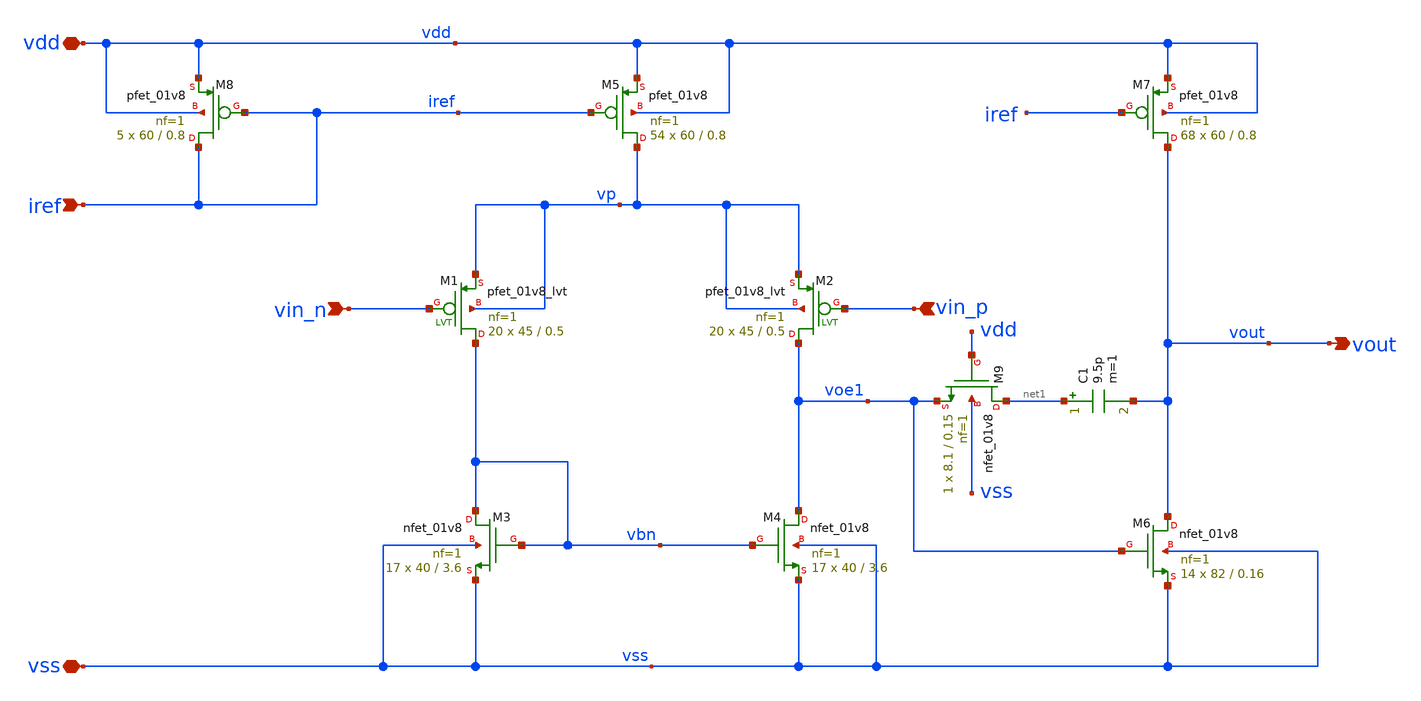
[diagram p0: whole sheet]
** sch_path: TpFinal/Mis Simulaciones/opamp.sch
**.subckt opamp vdd vss vin_n vin_p iref vout
*.iopin vdd
*.iopin vss
*.ipin vin_n
*.ipin vin_p
*.ipin iref
*.opin vout
XM3 vbn vbn vss vss sky130_fd_pr__nfet_01v8 L=3.6 W=40 nf=1 ad='W * 0.29' as='W * 0.29' pd='2 * (W + 0.29)'
+ ps='2 * (W + 0.29)' nrd='0.29 / W' nrs='0.29 / W' sa=0 sb=0 sd=0 mult=17 m=17
XM4 voe1 vbn vss vss sky130_fd_pr__nfet_01v8 L=3.6 W=40 nf=1 ad='W * 0.29' as='W * 0.29' pd='2 * (W + 0.29)'
+ ps='2 * (W + 0.29)' nrd='0.29 / W' nrs='0.29 / W' sa=0 sb=0 sd=0 mult=17 m=17
XM5 vp iref vdd vdd sky130_fd_pr__pfet_01v8 L=0.8 W=60 nf=1 ad='W * 0.29' as='W * 0.29' pd='2 * (W + 0.29)'
+ ps='2 * (W + 0.29)' nrd='0.29 / W' nrs='0.29 / W' sa=0 sb=0 sd=0 mult=54 m=54
XM7 vout iref vdd vdd sky130_fd_pr__pfet_01v8 L=0.8 W=60 nf=1 ad='W * 0.29' as='W * 0.29' pd='2 * (W + 0.29)'
+ ps='2 * (W + 0.29)' nrd='0.29 / W' nrs='0.29 / W' sa=0 sb=0 sd=0 mult=68 m=68
XM8 iref iref vdd vdd sky130_fd_pr__pfet_01v8 L=0.8 W=60 nf=1 ad='W * 0.29' as='W * 0.29' pd='2 * (W + 0.29)'
+ ps='2 * (W + 0.29)' nrd='0.29 / W' nrs='0.29 / W' sa=0 sb=0 sd=0 mult=5 m=5
XM9 net1 vdd voe1 vss sky130_fd_pr__nfet_01v8 L=0.15 W=8.1 nf=1 ad='W * 0.29' as='W * 0.29' pd='2 * (W + 0.29)'
+ ps='2 * (W + 0.29)' nrd='0.29 / W' nrs='0.29 / W' sa=0 sb=0 sd=0 mult=1 m=1
XM6 vout voe1 vss vss sky130_fd_pr__nfet_01v8 L=0.16 W=82 nf=1 ad='W * 0.29' as='W * 0.29' pd='2 * (W + 0.29)'
+ ps='2 * (W + 0.29)' nrd='0.29 / W' nrs='0.29 / W' sa=0 sb=0 sd=0 mult=14 m=14
XM1 vbn vin_n vp vp sky130_fd_pr__pfet_01v8_lvt L=0.5 W=45 nf=1 ad='int((nf+1)/2) * W/nf * 0.29' as='int((nf+2)/2) * W/nf * 0.29'
+ pd='2*int((nf+1)/2) * (W/nf + 0.29)' ps='2*int((nf+2)/2) * (W/nf + 0.29)' nrd='0.29 / W' nrs='0.29 / W'
+ sa=0 sb=0 sd=0 mult=20 m=20
XM2 voe1 vin_p vp vp sky130_fd_pr__pfet_01v8_lvt L=0.5 W=45 nf=1 ad='int((nf+1)/2) * W/nf * 0.29' as='int((nf+2)/2) * W/nf * 0.29'
+ pd='2*int((nf+1)/2) * (W/nf + 0.29)' ps='2*int((nf+2)/2) * (W/nf + 0.29)' nrd='0.29 / W' nrs='0.29 / W'
+ sa=0 sb=0 sd=0 mult=20 m=20
C1 net1 vout 9.5p m=1
**.ends
.end
